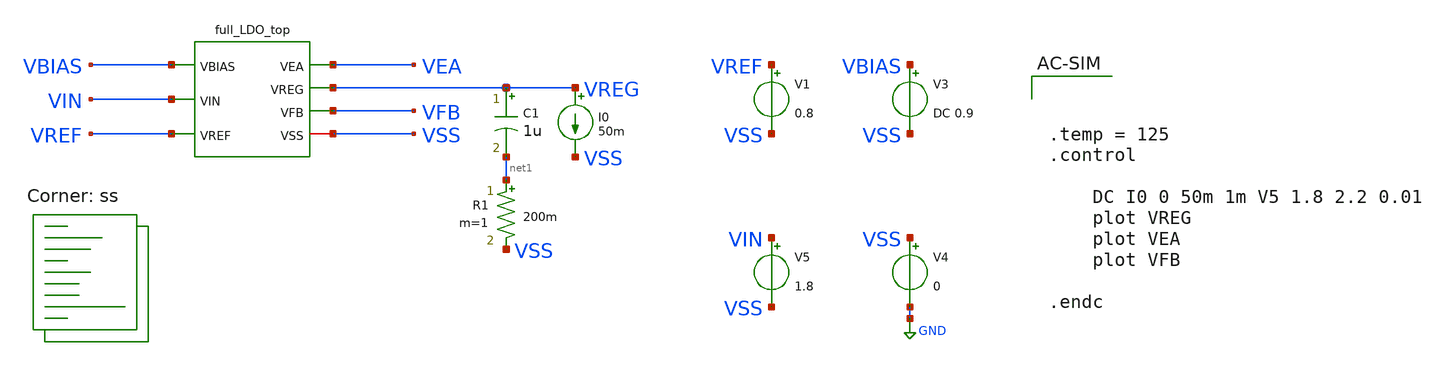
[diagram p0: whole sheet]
** sch_path: LDO_UVLO_Design/testbench/tb_LDO_1/load-line-analysis.sch
**.subckt load-line-analysis
x1 VBIAS VIN VREF VEA VREG VFB VSS full_LDO_top
V1 VREF VSS 0.8
V3 VBIAS VSS DC 0.9
V4 VSS GND 0
V5 VIN VSS 1.8
I0 VREG VSS 50m
C1 VREG net1 1u m=1
R1 net1 VSS 200m m=1
**** begin user architecture code
.lib $::SKYWATER_MODELS/sky130.lib.spice ss



.temp = 125
.control

	DC I0 0 50m 1m V5 1.8 2.2 0.01
	plot VREG
	plot VEA
	plot VFB

.endc


**** end user architecture code
**.ends

* expanding   symbol:  ldo-sky130A-its/LDO_UVLO_Design/schematics/full_LDO_top.sym # of pins=7
** sym_path: LDO_UVLO_Design/schematics/full_LDO_top.sym
** sch_path: LDO_UVLO_Design/schematics/full_LDO_top.sch
.subckt full_LDO_top VBIAS VIN VREF VEA VREG VFB VSS
*.ipin VREF
*.iopin VSS
*.ipin VIN
*.ipin VBIAS
*.opin VEA
*.opin VREG
*.opin VFB
x1 VIN VBIAS VFB VREF VEA VSS error_amplifier
XM1 VREG VEA VIN VIN sky130_fd_pr__pfet_01v8 L=0.18 W=597 nf=120 ad='int((nf+1)/2) * W/nf * 0.29' as='int((nf+2)/2) * W/nf * 0.29'
+ pd='2*int((nf+1)/2) * (W/nf + 0.29)' ps='2*int((nf+2)/2) * (W/nf + 0.29)' nrd='0.29 / W' nrs='0.29 / W'
+ sa=0 sb=0 sd=0 mult=2 m=2
XR1 VFB VREG VSS sky130_fd_pr__res_xhigh_po W=1 L=100 mult=1 m=1
XR2 VSS VFB VSS sky130_fd_pr__res_xhigh_po W=1 L=100 mult=1 m=1
.ends


* expanding   symbol:  ldo-sky130A-its/LDO_UVLO_Design/schematics/error_amplifier.sym # of pins=6
** sym_path: LDO_UVLO_Design/schematics/error_amplifier.sym
** sch_path: LDO_UVLO_Design/schematics/error_amplifier.sch
.subckt error_amplifier VDD VBIAS VP VN OUT VSS
*.iopin VDD
*.iopin VSS
*.ipin VBIAS
*.ipin VP
*.ipin VN
*.opin OUT
XM1 net2 net2 VSS VSS sky130_fd_pr__nfet_01v8 L=1.5 W=12 nf=1 ad='int((nf+1)/2) * W/nf * 0.29' as='int((nf+2)/2) * W/nf * 0.29'
+ pd='2*int((nf+1)/2) * (W/nf + 0.29)' ps='2*int((nf+2)/2) * (W/nf + 0.29)' nrd='0.29 / W' nrs='0.29 / W'
+ sa=0 sb=0 sd=0 mult=1 m=1
XM2 net1 net1 VSS VSS sky130_fd_pr__nfet_01v8 L=1.5 W=12 nf=1 ad='int((nf+1)/2) * W/nf * 0.29' as='int((nf+2)/2) * W/nf * 0.29'
+ pd='2*int((nf+1)/2) * (W/nf + 0.29)' ps='2*int((nf+2)/2) * (W/nf + 0.29)' nrd='0.29 / W' nrs='0.29 / W'
+ sa=0 sb=0 sd=0 mult=1 m=1
XM3 net2 VP net4 VDD sky130_fd_pr__pfet_01v8 L=1.5 W=12 nf=1 ad='int((nf+1)/2) * W/nf * 0.29' as='int((nf+2)/2) * W/nf * 0.29'
+ pd='2*int((nf+1)/2) * (W/nf + 0.29)' ps='2*int((nf+2)/2) * (W/nf + 0.29)' nrd='0.29 / W' nrs='0.29 / W'
+ sa=0 sb=0 sd=0 mult=1 m=1
XM4 net1 VN net4 VDD sky130_fd_pr__pfet_01v8 L=1.5 W=12 nf=1 ad='int((nf+1)/2) * W/nf * 0.29' as='int((nf+2)/2) * W/nf * 0.29'
+ pd='2*int((nf+1)/2) * (W/nf + 0.29)' ps='2*int((nf+2)/2) * (W/nf + 0.29)' nrd='0.29 / W' nrs='0.29 / W'
+ sa=0 sb=0 sd=0 mult=1 m=1
XM7 net3 net1 VSS VSS sky130_fd_pr__nfet_01v8 L=1.5 W=12 nf=1 ad='int((nf+1)/2) * W/nf * 0.29' as='int((nf+2)/2) * W/nf * 0.29'
+ pd='2*int((nf+1)/2) * (W/nf + 0.29)' ps='2*int((nf+2)/2) * (W/nf + 0.29)' nrd='0.29 / W' nrs='0.29 / W'
+ sa=0 sb=0 sd=0 mult=1 m=1
XM8 OUT net2 VSS VSS sky130_fd_pr__nfet_01v8 L=1.5 W=12 nf=1 ad='int((nf+1)/2) * W/nf * 0.29' as='int((nf+2)/2) * W/nf * 0.29'
+ pd='2*int((nf+1)/2) * (W/nf + 0.29)' ps='2*int((nf+2)/2) * (W/nf + 0.29)' nrd='0.29 / W' nrs='0.29 / W'
+ sa=0 sb=0 sd=0 mult=1 m=1
XM9 net3 net3 VDD VDD sky130_fd_pr__pfet_01v8 L=1.5 W=12 nf=1 ad='int((nf+1)/2) * W/nf * 0.29' as='int((nf+2)/2) * W/nf * 0.29'
+ pd='2*int((nf+1)/2) * (W/nf + 0.29)' ps='2*int((nf+2)/2) * (W/nf + 0.29)' nrd='0.29 / W' nrs='0.29 / W'
+ sa=0 sb=0 sd=0 mult=1 m=1
XM10 OUT net3 VDD VDD sky130_fd_pr__pfet_01v8 L=1.5 W=12 nf=1 ad='int((nf+1)/2) * W/nf * 0.29' as='int((nf+2)/2) * W/nf * 0.29'
+ pd='2*int((nf+1)/2) * (W/nf + 0.29)' ps='2*int((nf+2)/2) * (W/nf + 0.29)' nrd='0.29 / W' nrs='0.29 / W'
+ sa=0 sb=0 sd=0 mult=1 m=1
XM11 net4 VBIAS VDD VDD sky130_fd_pr__pfet_01v8 L=1.5 W=12 nf=1 ad='int((nf+1)/2) * W/nf * 0.29' as='int((nf+2)/2) * W/nf * 0.29'
+ pd='2*int((nf+1)/2) * (W/nf + 0.29)' ps='2*int((nf+2)/2) * (W/nf + 0.29)' nrd='0.29 / W' nrs='0.29 / W'
+ sa=0 sb=0 sd=0 mult=1 m=1
.ends

.GLOBAL GND
.end
